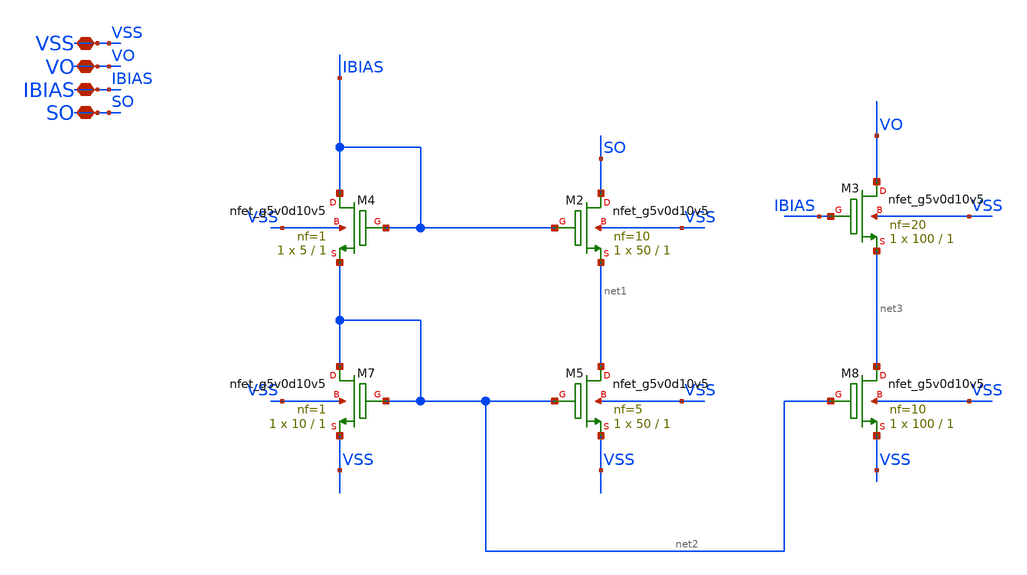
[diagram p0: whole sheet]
** sch_path: xschem/xschem_BGR_Top/Current_mirror_jaffar.sch
**.subckt Current_mirror_jaffar VSS VO IBIAS SO
*.iopin VSS
*.iopin VO
*.iopin IBIAS
*.iopin SO
XM2 SO IBIAS net1 VSS sky130_fd_pr__nfet_g5v0d10v5 L=1 W=50 nf=10 ad='int((nf+1)/2) * W/nf * 0.29' as='int((nf+2)/2) * W/nf * 0.29'
+ pd='2*int((nf+1)/2) * (W/nf + 0.29)' ps='2*int((nf+2)/2) * (W/nf + 0.29)' nrd='0.29 / W' nrs='0.29 / W'
+ sa=0 sb=0 sd=0 mult=1 m=1
XM3 VO IBIAS net3 VSS sky130_fd_pr__nfet_g5v0d10v5 L=1 W=100 nf=20 ad='int((nf+1)/2) * W/nf * 0.29' as='int((nf+2)/2) * W/nf * 0.29'
+ pd='2*int((nf+1)/2) * (W/nf + 0.29)' ps='2*int((nf+2)/2) * (W/nf + 0.29)' nrd='0.29 / W' nrs='0.29 / W'
+ sa=0 sb=0 sd=0 mult=1 m=1
XM4 IBIAS IBIAS net2 VSS sky130_fd_pr__nfet_g5v0d10v5 L=1 W=5 nf=1 ad='int((nf+1)/2) * W/nf * 0.29' as='int((nf+2)/2) * W/nf * 0.29'
+ pd='2*int((nf+1)/2) * (W/nf + 0.29)' ps='2*int((nf+2)/2) * (W/nf + 0.29)' nrd='0.29 / W' nrs='0.29 / W'
+ sa=0 sb=0 sd=0 mult=1 m=1
XM5 net1 net2 VSS VSS sky130_fd_pr__nfet_g5v0d10v5 L=1 W=50 nf=5 ad='int((nf+1)/2) * W/nf * 0.29' as='int((nf+2)/2) * W/nf * 0.29'
+ pd='2*int((nf+1)/2) * (W/nf + 0.29)' ps='2*int((nf+2)/2) * (W/nf + 0.29)' nrd='0.29 / W' nrs='0.29 / W'
+ sa=0 sb=0 sd=0 mult=1 m=1
XM7 net2 net2 VSS VSS sky130_fd_pr__nfet_g5v0d10v5 L=1 W=10 nf=1 ad='int((nf+1)/2) * W/nf * 0.29' as='int((nf+2)/2) * W/nf * 0.29'
+ pd='2*int((nf+1)/2) * (W/nf + 0.29)' ps='2*int((nf+2)/2) * (W/nf + 0.29)' nrd='0.29 / W' nrs='0.29 / W'
+ sa=0 sb=0 sd=0 mult=1 m=1
XM8 net3 net2 VSS VSS sky130_fd_pr__nfet_g5v0d10v5 L=1 W=100 nf=10 ad='int((nf+1)/2) * W/nf * 0.29' as='int((nf+2)/2) * W/nf * 0.29'
+ pd='2*int((nf+1)/2) * (W/nf + 0.29)' ps='2*int((nf+2)/2) * (W/nf + 0.29)' nrd='0.29 / W' nrs='0.29 / W'
+ sa=0 sb=0 sd=0 mult=1 m=1
**.ends
.end
